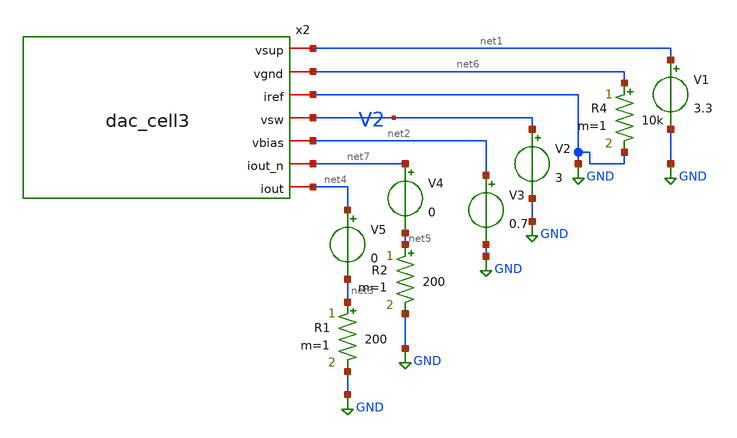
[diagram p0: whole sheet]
** sch_path: dev/dac_cell3/tb/tb_dac_cell3_op.sch
**.subckt tb_dac_cell3_op
V1 net1 GND 3.3
V2 V2 GND 3
V3 net2 GND 0.7
V4 net7 net5 0
V5 net4 net3 0
R1 net3 GND 200 m=1
R2 net5 GND 200 m=1
R4 net6 GND 10k m=1
x2 net1 net6 GND V2 net2 net7 net4 dac_cell3
**** begin user architecture code


.lib "/usr/share/pdk/sky130A/libs.tech/ngspice/sky130.lib.spice" tt
.param mc_mm_switch=0
.param mc_pr_switch=0
*** ANALYSIS TO DO

.op
.save V2 @m.x1.xm1.msky130_fd_pr__pfet_g5v0d10v5[id] @m.x1.xm2.msky130_fd_pr__pfet_g5v0d10v5[id] @m.x1.xm3.msky130_fd_pr__pfet_g5v0d10v5[id] @m.x1.xm4.msky130_fd_pr__pfet_g5v0d10v5[id]


.control
set wr_vecnames
set wr_singlescale

run
******** results filename  ************ nodes to write
wrdata $DEV_PATH/res/dac_cell3_op.res V2 @m.x1.xm1.msky130_fd_pr__pfet_g5v0d10v5[id]
+ @m.x1.xm2.msky130_fd_pr__pfet_g5v0d10v5[id] @m.x1.xm3.msky130_fd_pr__pfet_g5v0d10v5[id] @m.x1.xm4.msky130_fd_pr__pfet_g5v0d10v5[id]
.endc


**** end user architecture code
**.ends

* expanding   symbol:  dac_cell3.sym # of pins=7
** sym_path: dev/dac_cell3/tb/dac_cell3.sym
** sch_path: dev/dac_cell3/tb/dac_cell3.sch
.subckt dac_cell3 vsup vgnd iref vsw vbias iout_n iout
*.iopin vsup
*.iopin vgnd
*.iopin iref
*.iopin vsw
*.iopin iout
*.iopin iout_n
*.iopin vbias
XM1 iref iref vsup vsup sky130_fd_pr__pfet_g5v0d10v5 L=1 W=1 nf=1 ad='int((nf+1)/2) * W/nf * 0.29' as='int((nf+2)/2) * W/nf * 0.29'
+ pd='2*int((nf+1)/2) * (W/nf + 0.29)' ps='2*int((nf+2)/2) * (W/nf + 0.29)' nrd='0.29 / W' nrs='0.29 / W'
+ sa=0 sb=0 sd=0 mult=1 m=1
XM2 sourceM3M4 iref sourceM2 vsup sky130_fd_pr__pfet_g5v0d10v5 L=1 W=4 nf=1 ad='int((nf+1)/2) * W/nf * 0.29'
+ as='int((nf+2)/2) * W/nf * 0.29' pd='2*int((nf+1)/2) * (W/nf + 0.29)' ps='2*int((nf+2)/2) * (W/nf + 0.29)'
+ nrd='0.29 / W' nrs='0.29 / W' sa=0 sb=0 sd=0 mult=1 m=1
XM3 iout vsw sourceM3M4 vsup sky130_fd_pr__pfet_g5v0d10v5 L=1 W=4 nf=1 ad='int((nf+1)/2) * W/nf * 0.29'
+ as='int((nf+2)/2) * W/nf * 0.29' pd='2*int((nf+1)/2) * (W/nf + 0.29)' ps='2*int((nf+2)/2) * (W/nf + 0.29)'
+ nrd='0.29 / W' nrs='0.29 / W' sa=0 sb=0 sd=0 mult=1 m=1
XM4 iout_n vbias sourceM3M4 vsup sky130_fd_pr__pfet_g5v0d10v5 L=1 W=4 nf=1 ad='int((nf+1)/2) * W/nf * 0.29'
+ as='int((nf+2)/2) * W/nf * 0.29' pd='2*int((nf+1)/2) * (W/nf + 0.29)' ps='2*int((nf+2)/2) * (W/nf + 0.29)'
+ nrd='0.29 / W' nrs='0.29 / W' sa=0 sb=0 sd=0 mult=1 m=1
XR1 parR vsup vgnd sky130_fd_pr__res_xhigh_po_0p69 L=13 mult=1 m=1
XR2 sourceM2 parR vgnd sky130_fd_pr__res_xhigh_po_0p69 L=13 mult=1 m=1
XR3 parR vsup vgnd sky130_fd_pr__res_xhigh_po_0p69 L=13 mult=1 m=1
XR4 sourceM2 parR vgnd sky130_fd_pr__res_xhigh_po_0p69 L=13 mult=1 m=1
.ends

.GLOBAL GND
.end
